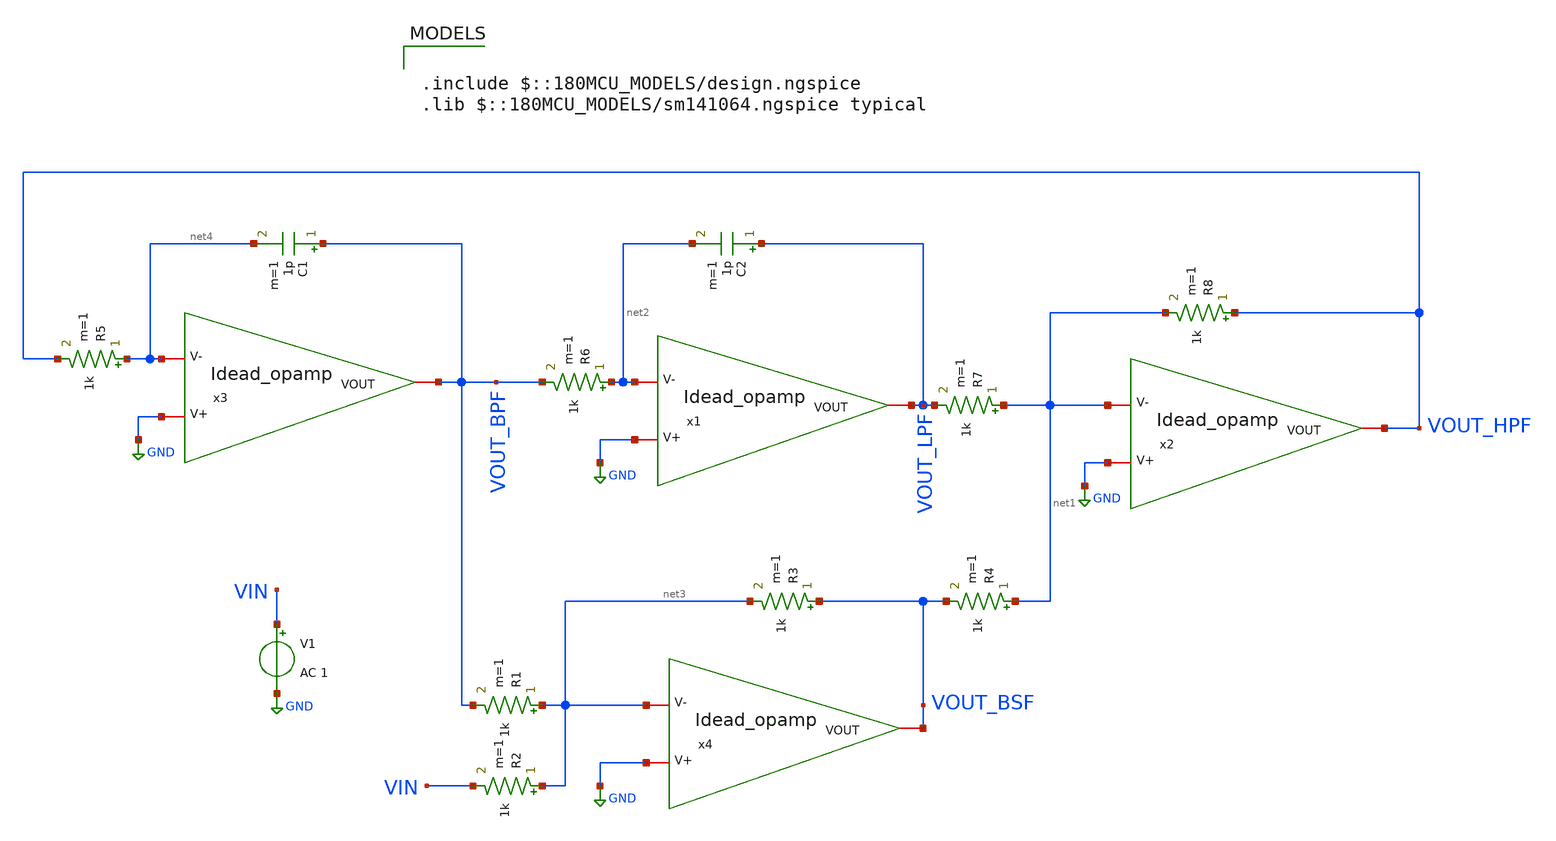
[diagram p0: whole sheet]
** sch_path: Design/Testbench.sch
**.subckt Testbench
x1 VOUT_LPF net2 GND Idead_opamp
x2 VOUT_HPF net1 GND Idead_opamp
x3 VOUT_BPF net4 GND Idead_opamp
x4 VOUT_BSF net3 GND Idead_opamp
R1 net3 VOUT_BPF 1k m=1
C1 VOUT_BPF net4 1p m=1
R2 net3 VIN 1k m=1
R3 VOUT_BSF net3 1k m=1
R4 net1 VOUT_BSF 1k m=1
R5 net4 VOUT_HPF 1k m=1
R6 net2 VOUT_BPF 1k m=1
R7 net1 VOUT_LPF 1k m=1
R8 VOUT_HPF net1 1k m=1
C2 VOUT_LPF net2 1p m=1
V1 VIN GND AC 1
**** begin user architecture code

.include sim_script.sim


.include $::180MCU_MODELS/design.ngspice
.lib $::180MCU_MODELS/sm141064.ngspice typical

**** end user architecture code
**.ends

* expanding   symbol:  Idead_opamp.sym # of pins=3
** sym_path: Design/Idead_opamp.sym
** sch_path: Design/Idead_opamp.sch
.subckt Idead_opamp VOUT V- V+
*.iopin V-
*.iopin V+
*.iopin VOUT
E1 VOUT GND V+ V- 10000
.ends

.GLOBAL GND
.end
